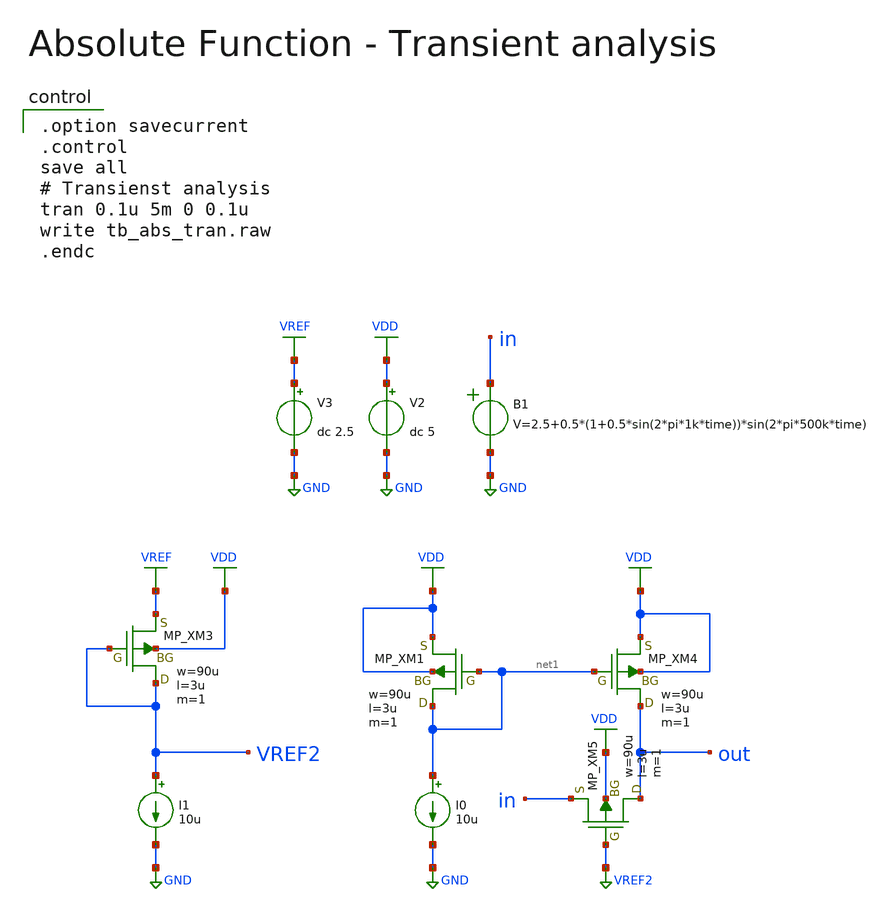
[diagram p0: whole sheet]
** sch_path: member_project/AM_Radio/Yamada3/xschem/tb_abs_tran.sch
**.subckt tb_abs_tran
V2 VDD GND dc 5
V3 VREF GND dc 2.5
B1 in GND V=2.5+0.5*(1+0.5*sin(2*pi*1k*time))*sin(2*pi*500k*time)
I0 net1 GND 10u
I1 VREF2 GND 10u
XM3 VREF2 VREF2 VREF VDD PMOS w=90u l=3u as=0 ad=0 ps=0 pd=0 nrd=0 nrs=0 m=1
XM1 net1 net1 VDD VDD PMOS w=90u l=3u as=0 ad=0 ps=0 pd=0 nrd=0 nrs=0 m=1
XM4 out net1 VDD VDD PMOS w=90u l=3u as=0 ad=0 ps=0 pd=0 nrd=0 nrs=0 m=1
XM5 out VREF2 in VDD PMOS w=90u l=3u as=0 ad=0 ps=0 pd=0 nrd=0 nrs=0 m=1
**** begin user architecture code

.option savecurrent
.control
save all
# Transienst analysis
tran 0.1u 5m 0 0.1u
write tb_abs_tran.raw
.endc

 .include $::LIB/ip62_models
**** end user architecture code
**.ends
.GLOBAL GND
.GLOBAL VDD
.GLOBAL VREF
.GLOBAL VREF2
.end
